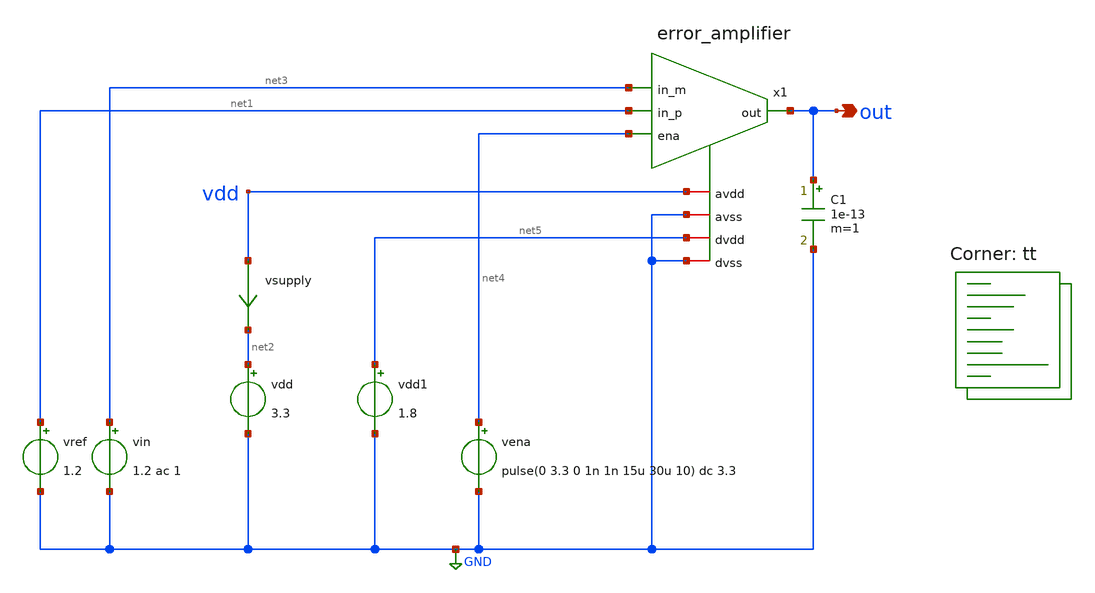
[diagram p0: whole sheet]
** sch_path: xschem/error_amplifier_tb.sch
**.subckt error_amplifier_tb out
*.opin out
x1 net4 net5 out net3 net1 GND vdd GND error_amplifier
vdd net2 GND 3.3
vref net1 GND 1.2
vin net3 GND 1.2 ac 1
vsupply vdd net2 0
.save i(vsupply)
C1 out GND 1e-13 m=1
vena net4 GND pulse(0 3.3 0 1n 1n 15u 30u 10) dc 3.3
vdd1 net5 GND 1.8
**** begin user architecture code

* ngspice control
.param W=100
.option savecurrents
.control
save all
op
write error_amplifier_tb.raw
set appendwrite
* dc vdd 0 3.3 10m
* plot v(out)

tran 100n 200u
plot x1.vbn x1.vcp x1.vbp vdd
plot i(vsupply)

dc vin 0 3.3 10m
plot v(out)

ac dec 10 10 1e9
set units=degrees
plot db(out)
plot ph(out)

.endc


.lib $::SKYWATER_MODELS/sky130.lib.spice tt
**** end user architecture code
**.ends

* expanding   symbol:  error_amplifier.sym # of pins=8
** sym_path: xschem/error_amplifier.sym
** sch_path: xschem/error_amplifier.sch
.subckt error_amplifier ena dvdd out in_m in_p dvss avdd avss
*.iopin avdd
*.iopin avss
*.ipin in_m
*.ipin in_p
*.opin out
*.ipin ena
*.iopin dvdd
*.iopin dvss
XM1 vbn vbn avss avss sky130_fd_pr__nfet_g5v0d10v5 L=10 W=1 nf=1 ad='int((nf+1)/2) * W/nf * 0.29' as='int((nf+2)/2) * W/nf * 0.29'
+ pd='2*int((nf+1)/2) * (W/nf + 0.29)' ps='2*int((nf+2)/2) * (W/nf + 0.29)' nrd='0.29 / W' nrs='0.29 / W'
+ sa=0 sb=0 sd=0 mult=1 m=1
XM3 vcp vbn net6 avss sky130_fd_pr__nfet_g5v0d10v5 L=10 W=1 nf=1 ad='int((nf+1)/2) * W/nf * 0.29' as='int((nf+2)/2) * W/nf * 0.29'
+ pd='2*int((nf+1)/2) * (W/nf + 0.29)' ps='2*int((nf+2)/2) * (W/nf + 0.29)' nrd='0.29 / W' nrs='0.29 / W'
+ sa=0 sb=0 sd=0 mult=4 m=4
XM5 vbp vbp avdd avdd sky130_fd_pr__pfet_g5v0d10v5 L=10 W=1 nf=1 ad='int((nf+1)/2) * W/nf * 0.29' as='int((nf+2)/2) * W/nf * 0.29'
+ pd='2*int((nf+1)/2) * (W/nf + 0.29)' ps='2*int((nf+2)/2) * (W/nf + 0.29)' nrd='0.29 / W' nrs='0.29 / W'
+ sa=0 sb=0 sd=0 mult=2 m=2
XM26 net4 vbp avdd avdd sky130_fd_pr__pfet_g5v0d10v5 L=10 W=1 nf=1 ad='int((nf+1)/2) * W/nf * 0.29' as='int((nf+2)/2) * W/nf * 0.29'
+ pd='2*int((nf+1)/2) * (W/nf + 0.29)' ps='2*int((nf+2)/2) * (W/nf + 0.29)' nrd='0.29 / W' nrs='0.29 / W'
+ sa=0 sb=0 sd=0 mult=6 m=6
XM27 net5 vbp avdd avdd sky130_fd_pr__pfet_g5v0d10v5 L=10 W=1 nf=1 ad='int((nf+1)/2) * W/nf * 0.29' as='int((nf+2)/2) * W/nf * 0.29'
+ pd='2*int((nf+1)/2) * (W/nf + 0.29)' ps='2*int((nf+2)/2) * (W/nf + 0.29)' nrd='0.29 / W' nrs='0.29 / W'
+ sa=0 sb=0 sd=0 mult=6 m=6
XM28 net3 vcp net4 avdd sky130_fd_pr__pfet_g5v0d10v5 L=2 W=1 nf=1 ad='int((nf+1)/2) * W/nf * 0.29' as='int((nf+2)/2) * W/nf * 0.29'
+ pd='2*int((nf+1)/2) * (W/nf + 0.29)' ps='2*int((nf+2)/2) * (W/nf + 0.29)' nrd='0.29 / W' nrs='0.29 / W'
+ sa=0 sb=0 sd=0 mult=1 m=1
XM29 v_cascode vcp net5 avdd sky130_fd_pr__pfet_g5v0d10v5 L=2 W=1 nf=1 ad='int((nf+1)/2) * W/nf * 0.29'
+ as='int((nf+2)/2) * W/nf * 0.29' pd='2*int((nf+1)/2) * (W/nf + 0.29)' ps='2*int((nf+2)/2) * (W/nf + 0.29)'
+ nrd='0.29 / W' nrs='0.29 / W' sa=0 sb=0 sd=0 mult=1 m=1
XM30 net3 vcn net1 avss sky130_fd_pr__nfet_g5v0d10v5 L=2 W=1 nf=1 ad='int((nf+1)/2) * W/nf * 0.29' as='int((nf+2)/2) * W/nf * 0.29'
+ pd='2*int((nf+1)/2) * (W/nf + 0.29)' ps='2*int((nf+2)/2) * (W/nf + 0.29)' nrd='0.29 / W' nrs='0.29 / W'
+ sa=0 sb=0 sd=0 mult=1 m=1
XM31 v_cascode vcn net2 avss sky130_fd_pr__nfet_g5v0d10v5 L=2 W=1 nf=1 ad='int((nf+1)/2) * W/nf * 0.29'
+ as='int((nf+2)/2) * W/nf * 0.29' pd='2*int((nf+1)/2) * (W/nf + 0.29)' ps='2*int((nf+2)/2) * (W/nf + 0.29)'
+ nrd='0.29 / W' nrs='0.29 / W' sa=0 sb=0 sd=0 mult=1 m=1
XM32 net1 net3 avss avss sky130_fd_pr__nfet_g5v0d10v5 L=10 W=1 nf=1 ad='int((nf+1)/2) * W/nf * 0.29'
+ as='int((nf+2)/2) * W/nf * 0.29' pd='2*int((nf+1)/2) * (W/nf + 0.29)' ps='2*int((nf+2)/2) * (W/nf + 0.29)'
+ nrd='0.29 / W' nrs='0.29 / W' sa=0 sb=0 sd=0 mult=3 m=3
XM33 net2 net3 avss avss sky130_fd_pr__nfet_g5v0d10v5 L=10 W=1 nf=1 ad='int((nf+1)/2) * W/nf * 0.29'
+ as='int((nf+2)/2) * W/nf * 0.29' pd='2*int((nf+1)/2) * (W/nf + 0.29)' ps='2*int((nf+2)/2) * (W/nf + 0.29)'
+ nrd='0.29 / W' nrs='0.29 / W' sa=0 sb=0 sd=0 mult=3 m=3
XM35 net11 vbp avdd avdd sky130_fd_pr__pfet_g5v0d10v5 L=10 W=1 nf=1 ad='int((nf+1)/2) * W/nf * 0.29'
+ as='int((nf+2)/2) * W/nf * 0.29' pd='2*int((nf+1)/2) * (W/nf + 0.29)' ps='2*int((nf+2)/2) * (W/nf + 0.29)'
+ nrd='0.29 / W' nrs='0.29 / W' sa=0 sb=0 sd=0 mult=2 m=2
XR3 avss net6 avss sky130_fd_pr__res_xhigh_po_0p35 L=180 mult=1 m=1
XM9 net13 v_cascode out avdd sky130_fd_pr__pfet_g5v0d10v5 L=10 W=1 nf=1 ad='int((nf+1)/2) * W/nf * 0.29'
+ as='int((nf+2)/2) * W/nf * 0.29' pd='2*int((nf+1)/2) * (W/nf + 0.29)' ps='2*int((nf+2)/2) * (W/nf + 0.29)'
+ nrd='0.29 / W' nrs='0.29 / W' sa=0 sb=0 sd=0 mult=1 m=1
XM8 out vbp avdd avdd sky130_fd_pr__pfet_g5v0d10v5 L=10 W=1 nf=1 ad='int((nf+1)/2) * W/nf * 0.29' as='int((nf+2)/2) * W/nf * 0.29'
+ pd='2*int((nf+1)/2) * (W/nf + 0.29)' ps='2*int((nf+2)/2) * (W/nf + 0.29)' nrd='0.29 / W' nrs='0.29 / W'
+ sa=0 sb=0 sd=0 mult=10 m=10
XM17 net8 vbp avdd avdd sky130_fd_pr__pfet_g5v0d10v5 L=10 W=1 nf=1 ad='int((nf+1)/2) * W/nf * 0.29' as='int((nf+2)/2) * W/nf * 0.29'
+ pd='2*int((nf+1)/2) * (W/nf + 0.29)' ps='2*int((nf+2)/2) * (W/nf + 0.29)' nrd='0.29 / W' nrs='0.29 / W'
+ sa=0 sb=0 sd=0 mult=1 m=1
XM19 net8 net8 net7 avss sky130_fd_pr__nfet_g5v0d10v5 L=0.5 W=1 nf=1 ad='int((nf+1)/2) * W/nf * 0.29'
+ as='int((nf+2)/2) * W/nf * 0.29' pd='2*int((nf+1)/2) * (W/nf + 0.29)' ps='2*int((nf+2)/2) * (W/nf + 0.29)'
+ nrd='0.29 / W' nrs='0.29 / W' sa=0 sb=0 sd=0 mult=6 m=6
XM20 net7 net8 avss avss sky130_fd_pr__nfet_g5v0d10v5 L=0.5 W=1 nf=1 ad='int((nf+1)/2) * W/nf * 0.29'
+ as='int((nf+2)/2) * W/nf * 0.29' pd='2*int((nf+1)/2) * (W/nf + 0.29)' ps='2*int((nf+2)/2) * (W/nf + 0.29)'
+ nrd='0.29 / W' nrs='0.29 / W' sa=0 sb=0 sd=0 mult=1 m=1
XM21 vcn vbp avdd avdd sky130_fd_pr__pfet_g5v0d10v5 L=10 W=1 nf=1 ad='int((nf+1)/2) * W/nf * 0.29' as='int((nf+2)/2) * W/nf * 0.29'
+ pd='2*int((nf+1)/2) * (W/nf + 0.29)' ps='2*int((nf+2)/2) * (W/nf + 0.29)' nrd='0.29 / W' nrs='0.29 / W'
+ sa=0 sb=0 sd=0 mult=5 m=5
XM36 vcn vcn net7 avss sky130_fd_pr__nfet_g5v0d10v5 L=2 W=1 nf=1 ad='int((nf+1)/2) * W/nf * 0.29' as='int((nf+2)/2) * W/nf * 0.29'
+ pd='2*int((nf+1)/2) * (W/nf + 0.29)' ps='2*int((nf+2)/2) * (W/nf + 0.29)' nrd='0.29 / W' nrs='0.29 / W'
+ sa=0 sb=0 sd=0 mult=1 m=1
XM6 net5 in_m net9 avss sky130_fd_pr__nfet_g5v0d10v5 L=0.5 W=1 nf=1 ad='int((nf+1)/2) * W/nf * 0.29'
+ as='int((nf+2)/2) * W/nf * 0.29' pd='2*int((nf+1)/2) * (W/nf + 0.29)' ps='2*int((nf+2)/2) * (W/nf + 0.29)'
+ nrd='0.29 / W' nrs='0.29 / W' sa=0 sb=0 sd=0 mult=1 m=1
XM7 net9 vbn avss avss sky130_fd_pr__nfet_g5v0d10v5 L=10 W=1 nf=1 ad='int((nf+1)/2) * W/nf * 0.29' as='int((nf+2)/2) * W/nf * 0.29'
+ pd='2*int((nf+1)/2) * (W/nf + 0.29)' ps='2*int((nf+2)/2) * (W/nf + 0.29)' nrd='0.29 / W' nrs='0.29 / W'
+ sa=0 sb=0 sd=0 mult=2 m=2
XM12 net4 in_p net9 avss sky130_fd_pr__nfet_g5v0d10v5 L=0.5 W=1 nf=1 ad='int((nf+1)/2) * W/nf * 0.29'
+ as='int((nf+2)/2) * W/nf * 0.29' pd='2*int((nf+1)/2) * (W/nf + 0.29)' ps='2*int((nf+2)/2) * (W/nf + 0.29)'
+ nrd='0.29 / W' nrs='0.29 / W' sa=0 sb=0 sd=0 mult=1 m=1
XM10 vstart vbn avss avss sky130_fd_pr__nfet_g5v0d10v5 L=1 W=10 nf=1 ad='int((nf+1)/2) * W/nf * 0.29'
+ as='int((nf+2)/2) * W/nf * 0.29' pd='2*int((nf+1)/2) * (W/nf + 0.29)' ps='2*int((nf+2)/2) * (W/nf + 0.29)'
+ nrd='0.29 / W' nrs='0.29 / W' sa=0 sb=0 sd=0 mult=1 m=1
XM11 vstart avss net10 avdd sky130_fd_pr__pfet_g5v0d10v5 L=20 W=1 nf=1 ad='int((nf+1)/2) * W/nf * 0.29'
+ as='int((nf+2)/2) * W/nf * 0.29' pd='2*int((nf+1)/2) * (W/nf + 0.29)' ps='2*int((nf+2)/2) * (W/nf + 0.29)'
+ nrd='0.29 / W' nrs='0.29 / W' sa=0 sb=0 sd=0 mult=1 m=1
XM2 vcp vcp vbp avdd sky130_fd_pr__pfet_g5v0d10v5 L=10 W=1 nf=1 ad='int((nf+1)/2) * W/nf * 0.29' as='int((nf+2)/2) * W/nf * 0.29'
+ pd='2*int((nf+1)/2) * (W/nf + 0.29)' ps='2*int((nf+2)/2) * (W/nf + 0.29)' nrd='0.29 / W' nrs='0.29 / W'
+ sa=0 sb=0 sd=0 mult=2 m=2
XM4 vbn vcp net11 avdd sky130_fd_pr__pfet_g5v0d10v5 L=10 W=1 nf=1 ad='int((nf+1)/2) * W/nf * 0.29' as='int((nf+2)/2) * W/nf * 0.29'
+ pd='2*int((nf+1)/2) * (W/nf + 0.29)' ps='2*int((nf+2)/2) * (W/nf + 0.29)' nrd='0.29 / W' nrs='0.29 / W'
+ sa=0 sb=0 sd=0 mult=2 m=2
XM13 vbp vstart avss avss sky130_fd_pr__nfet_g5v0d10v5 L=0.5 W=1 nf=1 ad='int((nf+1)/2) * W/nf * 0.29'
+ as='int((nf+2)/2) * W/nf * 0.29' pd='2*int((nf+1)/2) * (W/nf + 0.29)' ps='2*int((nf+2)/2) * (W/nf + 0.29)'
+ nrd='0.29 / W' nrs='0.29 / W' sa=0 sb=0 sd=0 mult=1 m=1
XM14 vcp vstart avss avss sky130_fd_pr__nfet_g5v0d10v5 L=0.5 W=1 nf=1 ad='int((nf+1)/2) * W/nf * 0.29'
+ as='int((nf+2)/2) * W/nf * 0.29' pd='2*int((nf+1)/2) * (W/nf + 0.29)' ps='2*int((nf+2)/2) * (W/nf + 0.29)'
+ nrd='0.29 / W' nrs='0.29 / W' sa=0 sb=0 sd=0 mult=1 m=1
XM15 net10 net10 net12 avdd sky130_fd_pr__pfet_g5v0d10v5 L=20 W=1 nf=1 ad='int((nf+1)/2) * W/nf * 0.29'
+ as='int((nf+2)/2) * W/nf * 0.29' pd='2*int((nf+1)/2) * (W/nf + 0.29)' ps='2*int((nf+2)/2) * (W/nf + 0.29)'
+ nrd='0.29 / W' nrs='0.29 / W' sa=0 sb=0 sd=0 mult=1 m=1
XM16 vbp v_ena avdd avdd sky130_fd_pr__pfet_g5v0d10v5 L=0.5 W=1 nf=1 ad='int((nf+1)/2) * W/nf * 0.29'
+ as='int((nf+2)/2) * W/nf * 0.29' pd='2*int((nf+1)/2) * (W/nf + 0.29)' ps='2*int((nf+2)/2) * (W/nf + 0.29)'
+ nrd='0.29 / W' nrs='0.29 / W' sa=0 sb=0 sd=0 mult=1 m=1
XM18 vcp v_ena avdd avdd sky130_fd_pr__pfet_g5v0d10v5 L=0.5 W=1 nf=1 ad='int((nf+1)/2) * W/nf * 0.29'
+ as='int((nf+2)/2) * W/nf * 0.29' pd='2*int((nf+1)/2) * (W/nf + 0.29)' ps='2*int((nf+2)/2) * (W/nf + 0.29)'
+ nrd='0.29 / W' nrs='0.29 / W' sa=0 sb=0 sd=0 mult=1 m=1
XM22 vbn v_ena_b avss avss sky130_fd_pr__nfet_g5v0d10v5 L=0.5 W=1 nf=1 ad='int((nf+1)/2) * W/nf * 0.29'
+ as='int((nf+2)/2) * W/nf * 0.29' pd='2*int((nf+1)/2) * (W/nf + 0.29)' ps='2*int((nf+2)/2) * (W/nf + 0.29)'
+ nrd='0.29 / W' nrs='0.29 / W' sa=0 sb=0 sd=0 mult=1 m=1
XM23 vcn v_ena_b avss avss sky130_fd_pr__nfet_g5v0d10v5 L=0.5 W=1 nf=1 ad='int((nf+1)/2) * W/nf * 0.29'
+ as='int((nf+2)/2) * W/nf * 0.29' pd='2*int((nf+1)/2) * (W/nf + 0.29)' ps='2*int((nf+2)/2) * (W/nf + 0.29)'
+ nrd='0.29 / W' nrs='0.29 / W' sa=0 sb=0 sd=0 mult=1 m=1
XM24 v_cascode v_ena_b avss avss sky130_fd_pr__nfet_g5v0d10v5 L=0.5 W=1 nf=1 ad='int((nf+1)/2) * W/nf * 0.29'
+ as='int((nf+2)/2) * W/nf * 0.29' pd='2*int((nf+1)/2) * (W/nf + 0.29)' ps='2*int((nf+2)/2) * (W/nf + 0.29)'
+ nrd='0.29 / W' nrs='0.29 / W' sa=0 sb=0 sd=0 mult=1 m=1
XM25 out v_ena_b avss avss sky130_fd_pr__nfet_g5v0d10v5 L=0.5 W=1 nf=1 ad='int((nf+1)/2) * W/nf * 0.29'
+ as='int((nf+2)/2) * W/nf * 0.29' pd='2*int((nf+1)/2) * (W/nf + 0.29)' ps='2*int((nf+2)/2) * (W/nf + 0.29)'
+ nrd='0.29 / W' nrs='0.29 / W' sa=0 sb=0 sd=0 mult=1 m=1
XM34 vstart v_ena_b avss avss sky130_fd_pr__nfet_g5v0d10v5 L=0.5 W=1 nf=1 ad='int((nf+1)/2) * W/nf * 0.29'
+ as='int((nf+2)/2) * W/nf * 0.29' pd='2*int((nf+1)/2) * (W/nf + 0.29)' ps='2*int((nf+2)/2) * (W/nf + 0.29)'
+ nrd='0.29 / W' nrs='0.29 / W' sa=0 sb=0 sd=0 mult=1 m=1
XM37 net12 v_ena_b avdd avdd sky130_fd_pr__pfet_g5v0d10v5 L=0.5 W=1 nf=1 ad='int((nf+1)/2) * W/nf * 0.29'
+ as='int((nf+2)/2) * W/nf * 0.29' pd='2*int((nf+1)/2) * (W/nf + 0.29)' ps='2*int((nf+2)/2) * (W/nf + 0.29)'
+ nrd='0.29 / W' nrs='0.29 / W' sa=0 sb=0 sd=0 mult=1 m=1
XM38 net13 vbn avss avss sky130_fd_pr__nfet_g5v0d10v5 L=10 W=1 nf=1 ad='int((nf+1)/2) * W/nf * 0.29'
+ as='int((nf+2)/2) * W/nf * 0.29' pd='2*int((nf+1)/2) * (W/nf + 0.29)' ps='2*int((nf+2)/2) * (W/nf + 0.29)'
+ nrd='0.29 / W' nrs='0.29 / W' sa=0 sb=0 sd=0 mult=2 m=2
XM39 out net13 avss avss sky130_fd_pr__nfet_g5v0d10v5 L=0.5 W=4 nf=1 ad='int((nf+1)/2) * W/nf * 0.29'
+ as='int((nf+2)/2) * W/nf * 0.29' pd='2*int((nf+1)/2) * (W/nf + 0.29)' ps='2*int((nf+2)/2) * (W/nf + 0.29)'
+ nrd='0.29 / W' nrs='0.29 / W' sa=0 sb=0 sd=0 mult=1 m=1
XM41 ena_b ena dvdd dvdd sky130_fd_pr__pfet_g5v0d10v5 L=0.5 W=2.5 nf=1 ad='int((nf+1)/2) * W/nf * 0.29'
+ as='int((nf+2)/2) * W/nf * 0.29' pd='2*int((nf+1)/2) * (W/nf + 0.29)' ps='2*int((nf+2)/2) * (W/nf + 0.29)'
+ nrd='0.29 / W' nrs='0.29 / W' sa=0 sb=0 sd=0 mult=1 m=1
XM42 ena_b ena dvss dvss sky130_fd_pr__nfet_g5v0d10v5 L=0.5 W=1 nf=1 ad='int((nf+1)/2) * W/nf * 0.29'
+ as='int((nf+2)/2) * W/nf * 0.29' pd='2*int((nf+1)/2) * (W/nf + 0.29)' ps='2*int((nf+2)/2) * (W/nf + 0.29)'
+ nrd='0.29 / W' nrs='0.29 / W' sa=0 sb=0 sd=0 mult=1 m=1
XM43 v_ena v_ena_b avdd avdd sky130_fd_pr__pfet_g5v0d10v5 L=0.5 W=2.5 nf=1 ad='int((nf+1)/2) * W/nf * 0.29'
+ as='int((nf+2)/2) * W/nf * 0.29' pd='2*int((nf+1)/2) * (W/nf + 0.29)' ps='2*int((nf+2)/2) * (W/nf + 0.29)'
+ nrd='0.29 / W' nrs='0.29 / W' sa=0 sb=0 sd=0 mult=1 m=1
XM44 v_ena ena_b avss avss sky130_fd_pr__nfet_g5v0d10v5 L=0.5 W=1 nf=1 ad='int((nf+1)/2) * W/nf * 0.29'
+ as='int((nf+2)/2) * W/nf * 0.29' pd='2*int((nf+1)/2) * (W/nf + 0.29)' ps='2*int((nf+2)/2) * (W/nf + 0.29)'
+ nrd='0.29 / W' nrs='0.29 / W' sa=0 sb=0 sd=0 mult=1 m=1
XM45 v_ena_b v_ena avdd avdd sky130_fd_pr__pfet_g5v0d10v5 L=0.5 W=2.5 nf=1 ad='int((nf+1)/2) * W/nf * 0.29'
+ as='int((nf+2)/2) * W/nf * 0.29' pd='2*int((nf+1)/2) * (W/nf + 0.29)' ps='2*int((nf+2)/2) * (W/nf + 0.29)'
+ nrd='0.29 / W' nrs='0.29 / W' sa=0 sb=0 sd=0 mult=1 m=1
XM46 v_ena_b ena avss avss sky130_fd_pr__nfet_g5v0d10v5 L=0.5 W=1 nf=1 ad='int((nf+1)/2) * W/nf * 0.29'
+ as='int((nf+2)/2) * W/nf * 0.29' pd='2*int((nf+1)/2) * (W/nf + 0.29)' ps='2*int((nf+2)/2) * (W/nf + 0.29)'
+ nrd='0.29 / W' nrs='0.29 / W' sa=0 sb=0 sd=0 mult=1 m=1
XC1 out v_cascode sky130_fd_pr__cap_mim_m3_1 W=6 L=6 MF=4 m=4
.ends

.GLOBAL GND
.end
